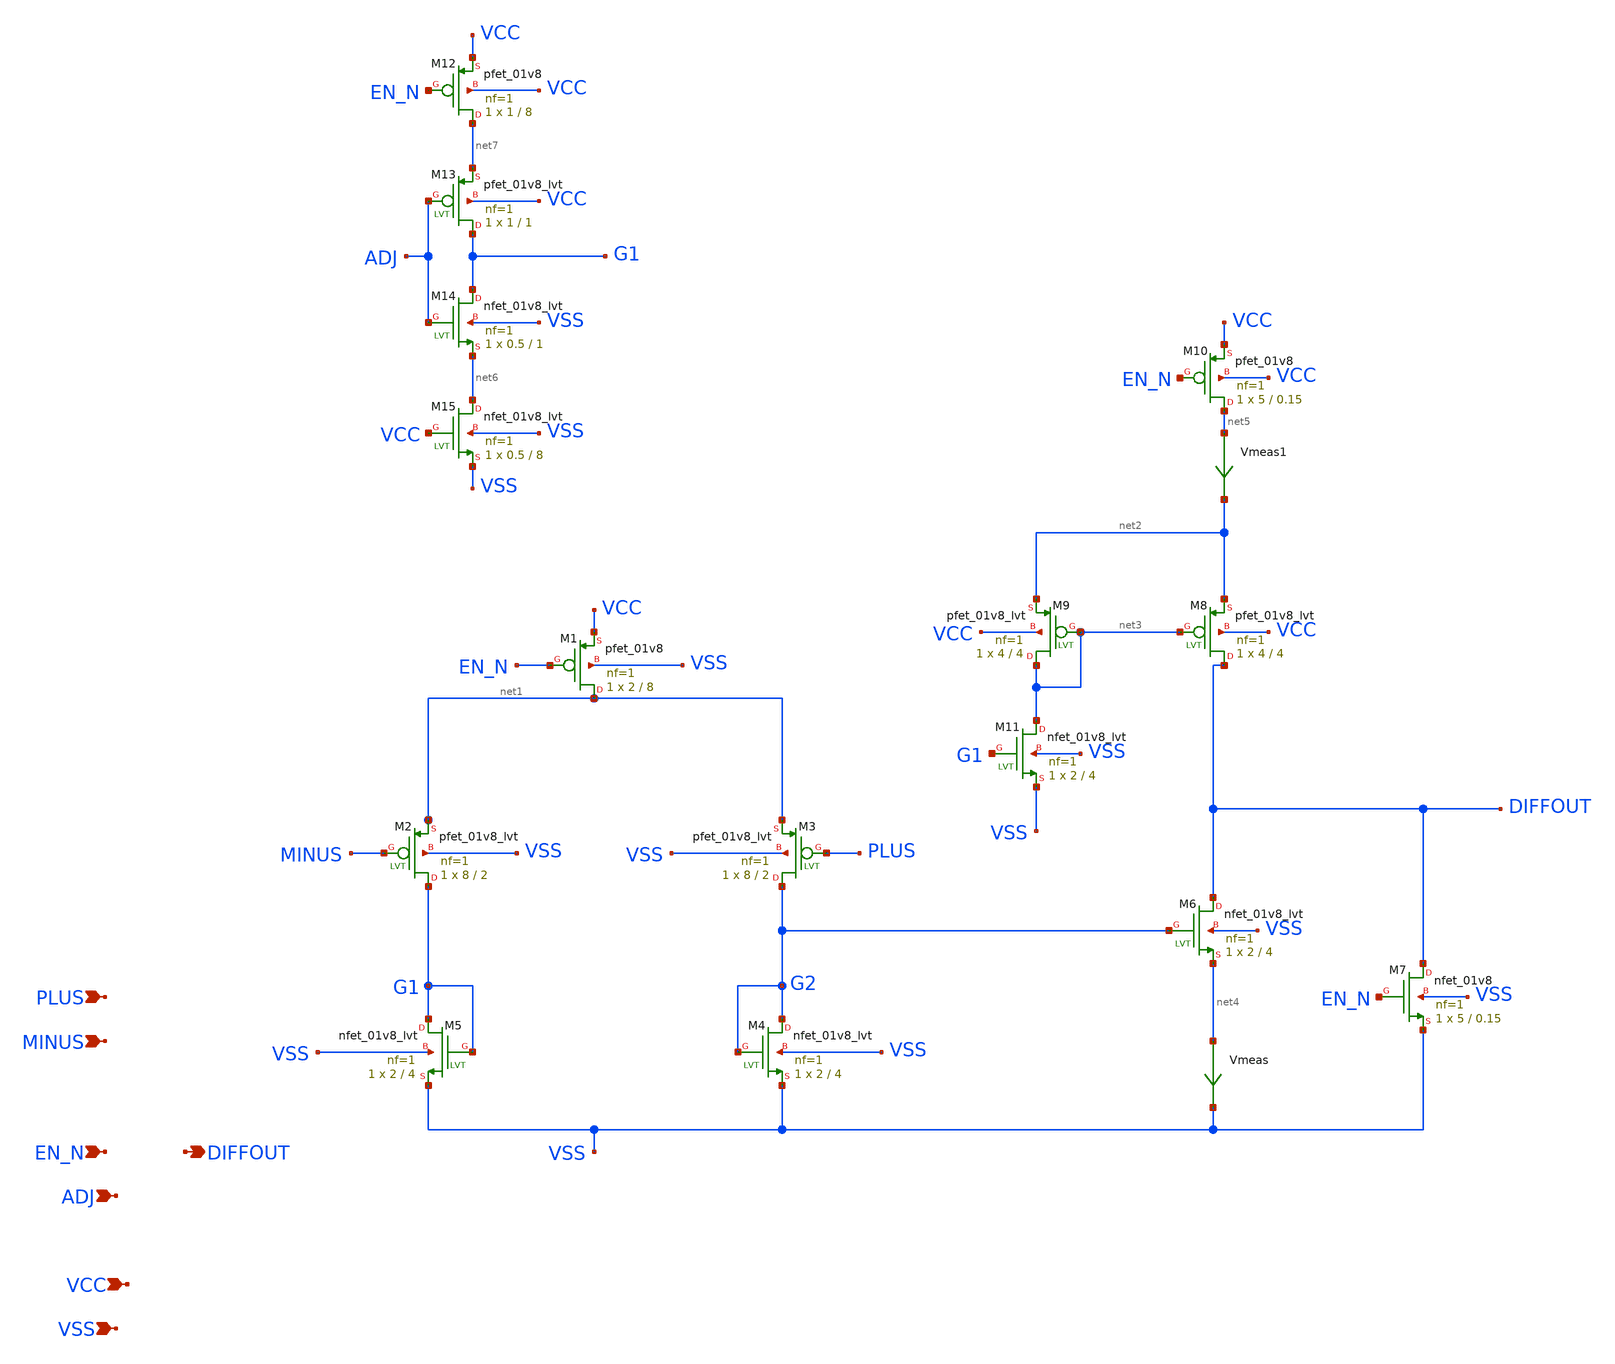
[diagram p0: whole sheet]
** sch_path: opamp.sch
**.subckt opamp PLUS MINUS VCC VSS EN_N ADJ DIFFOUT
*.ipin PLUS
*.ipin MINUS
*.ipin VCC
*.ipin VSS
*.ipin EN_N
*.ipin ADJ
*.opin DIFFOUT
XM1 net1 EN_N VCC VSS sky130_fd_pr__pfet_01v8 L=8 W=2 nf=1 ad='int((nf+1)/2) * W/nf * 0.29' as='int((nf+2)/2) * W/nf * 0.29'
+ pd='2*int((nf+1)/2) * (W/nf + 0.29)' ps='2*int((nf+2)/2) * (W/nf + 0.29)' nrd='0.29 / W' nrs='0.29 / W'
+ sa=0 sb=0 sd=0 mult=1 m=1
XM2 G1 MINUS net1 VSS sky130_fd_pr__pfet_01v8_lvt L=2 W=8 nf=1 ad='int((nf+1)/2) * W/nf * 0.29' as='int((nf+2)/2) * W/nf * 0.29'
+ pd='2*int((nf+1)/2) * (W/nf + 0.29)' ps='2*int((nf+2)/2) * (W/nf + 0.29)' nrd='0.29 / W' nrs='0.29 / W'
+ sa=0 sb=0 sd=0 mult=1 m=1
XM3 G2 PLUS net1 VSS sky130_fd_pr__pfet_01v8_lvt L=2 W=8 nf=1 ad='int((nf+1)/2) * W/nf * 0.29' as='int((nf+2)/2) * W/nf * 0.29'
+ pd='2*int((nf+1)/2) * (W/nf + 0.29)' ps='2*int((nf+2)/2) * (W/nf + 0.29)' nrd='0.29 / W' nrs='0.29 / W'
+ sa=0 sb=0 sd=0 mult=1 m=1
XM4 G2 G2 VSS VSS sky130_fd_pr__nfet_01v8_lvt L=4 W=2 nf=1 ad='int((nf+1)/2) * W/nf * 0.29' as='int((nf+2)/2) * W/nf * 0.29'
+ pd='2*int((nf+1)/2) * (W/nf + 0.29)' ps='2*int((nf+2)/2) * (W/nf + 0.29)' nrd='0.29 / W' nrs='0.29 / W'
+ sa=0 sb=0 sd=0 mult=1 m=1
XM5 G1 G1 VSS VSS sky130_fd_pr__nfet_01v8_lvt L=4 W=2 nf=1 ad='int((nf+1)/2) * W/nf * 0.29' as='int((nf+2)/2) * W/nf * 0.29'
+ pd='2*int((nf+1)/2) * (W/nf + 0.29)' ps='2*int((nf+2)/2) * (W/nf + 0.29)' nrd='0.29 / W' nrs='0.29 / W'
+ sa=0 sb=0 sd=0 mult=1 m=1
XM6 DIFFOUT G2 net4 VSS sky130_fd_pr__nfet_01v8_lvt L=4 W=2 nf=1 ad='int((nf+1)/2) * W/nf * 0.29' as='int((nf+2)/2) * W/nf * 0.29'
+ pd='2*int((nf+1)/2) * (W/nf + 0.29)' ps='2*int((nf+2)/2) * (W/nf + 0.29)' nrd='0.29 / W' nrs='0.29 / W'
+ sa=0 sb=0 sd=0 mult=1 m=1
XM7 DIFFOUT EN_N VSS VSS sky130_fd_pr__nfet_01v8 L=0.15 W=5 nf=1 ad='int((nf+1)/2) * W/nf * 0.29' as='int((nf+2)/2) * W/nf * 0.29'
+ pd='2*int((nf+1)/2) * (W/nf + 0.29)' ps='2*int((nf+2)/2) * (W/nf + 0.29)' nrd='0.29 / W' nrs='0.29 / W'
+ sa=0 sb=0 sd=0 mult=1 m=1
XM8 DIFFOUT net3 net2 VCC sky130_fd_pr__pfet_01v8_lvt L=4 W=4 nf=1 ad='int((nf+1)/2) * W/nf * 0.29' as='int((nf+2)/2) * W/nf * 0.29'
+ pd='2*int((nf+1)/2) * (W/nf + 0.29)' ps='2*int((nf+2)/2) * (W/nf + 0.29)' nrd='0.29 / W' nrs='0.29 / W'
+ sa=0 sb=0 sd=0 mult=1 m=1
XM9 net3 net3 net2 VCC sky130_fd_pr__pfet_01v8_lvt L=4 W=4 nf=1 ad='int((nf+1)/2) * W/nf * 0.29' as='int((nf+2)/2) * W/nf * 0.29'
+ pd='2*int((nf+1)/2) * (W/nf + 0.29)' ps='2*int((nf+2)/2) * (W/nf + 0.29)' nrd='0.29 / W' nrs='0.29 / W'
+ sa=0 sb=0 sd=0 mult=1 m=1
XM10 net5 EN_N VCC VCC sky130_fd_pr__pfet_01v8 L=0.15 W=5 nf=1 ad='int((nf+1)/2) * W/nf * 0.29' as='int((nf+2)/2) * W/nf * 0.29'
+ pd='2*int((nf+1)/2) * (W/nf + 0.29)' ps='2*int((nf+2)/2) * (W/nf + 0.29)' nrd='0.29 / W' nrs='0.29 / W'
+ sa=0 sb=0 sd=0 mult=1 m=1
XM11 net3 G1 VSS VSS sky130_fd_pr__nfet_01v8_lvt L=4 W=2 nf=1 ad='int((nf+1)/2) * W/nf * 0.29' as='int((nf+2)/2) * W/nf * 0.29'
+ pd='2*int((nf+1)/2) * (W/nf + 0.29)' ps='2*int((nf+2)/2) * (W/nf + 0.29)' nrd='0.29 / W' nrs='0.29 / W'
+ sa=0 sb=0 sd=0 mult=1 m=1
Vmeas net4 VSS 0
.save i(vmeas)
Vmeas1 net5 net2 0
.save i(vmeas1)
XM12 net7 EN_N VCC VCC sky130_fd_pr__pfet_01v8 L=8 W=1 nf=1 ad='int((nf+1)/2) * W/nf * 0.29' as='int((nf+2)/2) * W/nf * 0.29'
+ pd='2*int((nf+1)/2) * (W/nf + 0.29)' ps='2*int((nf+2)/2) * (W/nf + 0.29)' nrd='0.29 / W' nrs='0.29 / W'
+ sa=0 sb=0 sd=0 mult=1 m=1
XM13 G1 ADJ net7 VCC sky130_fd_pr__pfet_01v8_lvt L=1 W=1 nf=1 ad='int((nf+1)/2) * W/nf * 0.29' as='int((nf+2)/2) * W/nf * 0.29'
+ pd='2*int((nf+1)/2) * (W/nf + 0.29)' ps='2*int((nf+2)/2) * (W/nf + 0.29)' nrd='0.29 / W' nrs='0.29 / W'
+ sa=0 sb=0 sd=0 mult=1 m=1
XM14 G1 ADJ net6 VSS sky130_fd_pr__nfet_01v8_lvt L=1 W=0.5 nf=1 ad='int((nf+1)/2) * W/nf * 0.29' as='int((nf+2)/2) * W/nf * 0.29'
+ pd='2*int((nf+1)/2) * (W/nf + 0.29)' ps='2*int((nf+2)/2) * (W/nf + 0.29)' nrd='0.29 / W' nrs='0.29 / W'
+ sa=0 sb=0 sd=0 mult=1 m=1
XM15 net6 VCC VSS VSS sky130_fd_pr__nfet_01v8_lvt L=8 W=0.5 nf=1 ad='int((nf+1)/2) * W/nf * 0.29' as='int((nf+2)/2) * W/nf * 0.29'
+ pd='2*int((nf+1)/2) * (W/nf + 0.29)' ps='2*int((nf+2)/2) * (W/nf + 0.29)' nrd='0.29 / W' nrs='0.29 / W'
+ sa=0 sb=0 sd=0 mult=1 m=1
**.ends
.end
